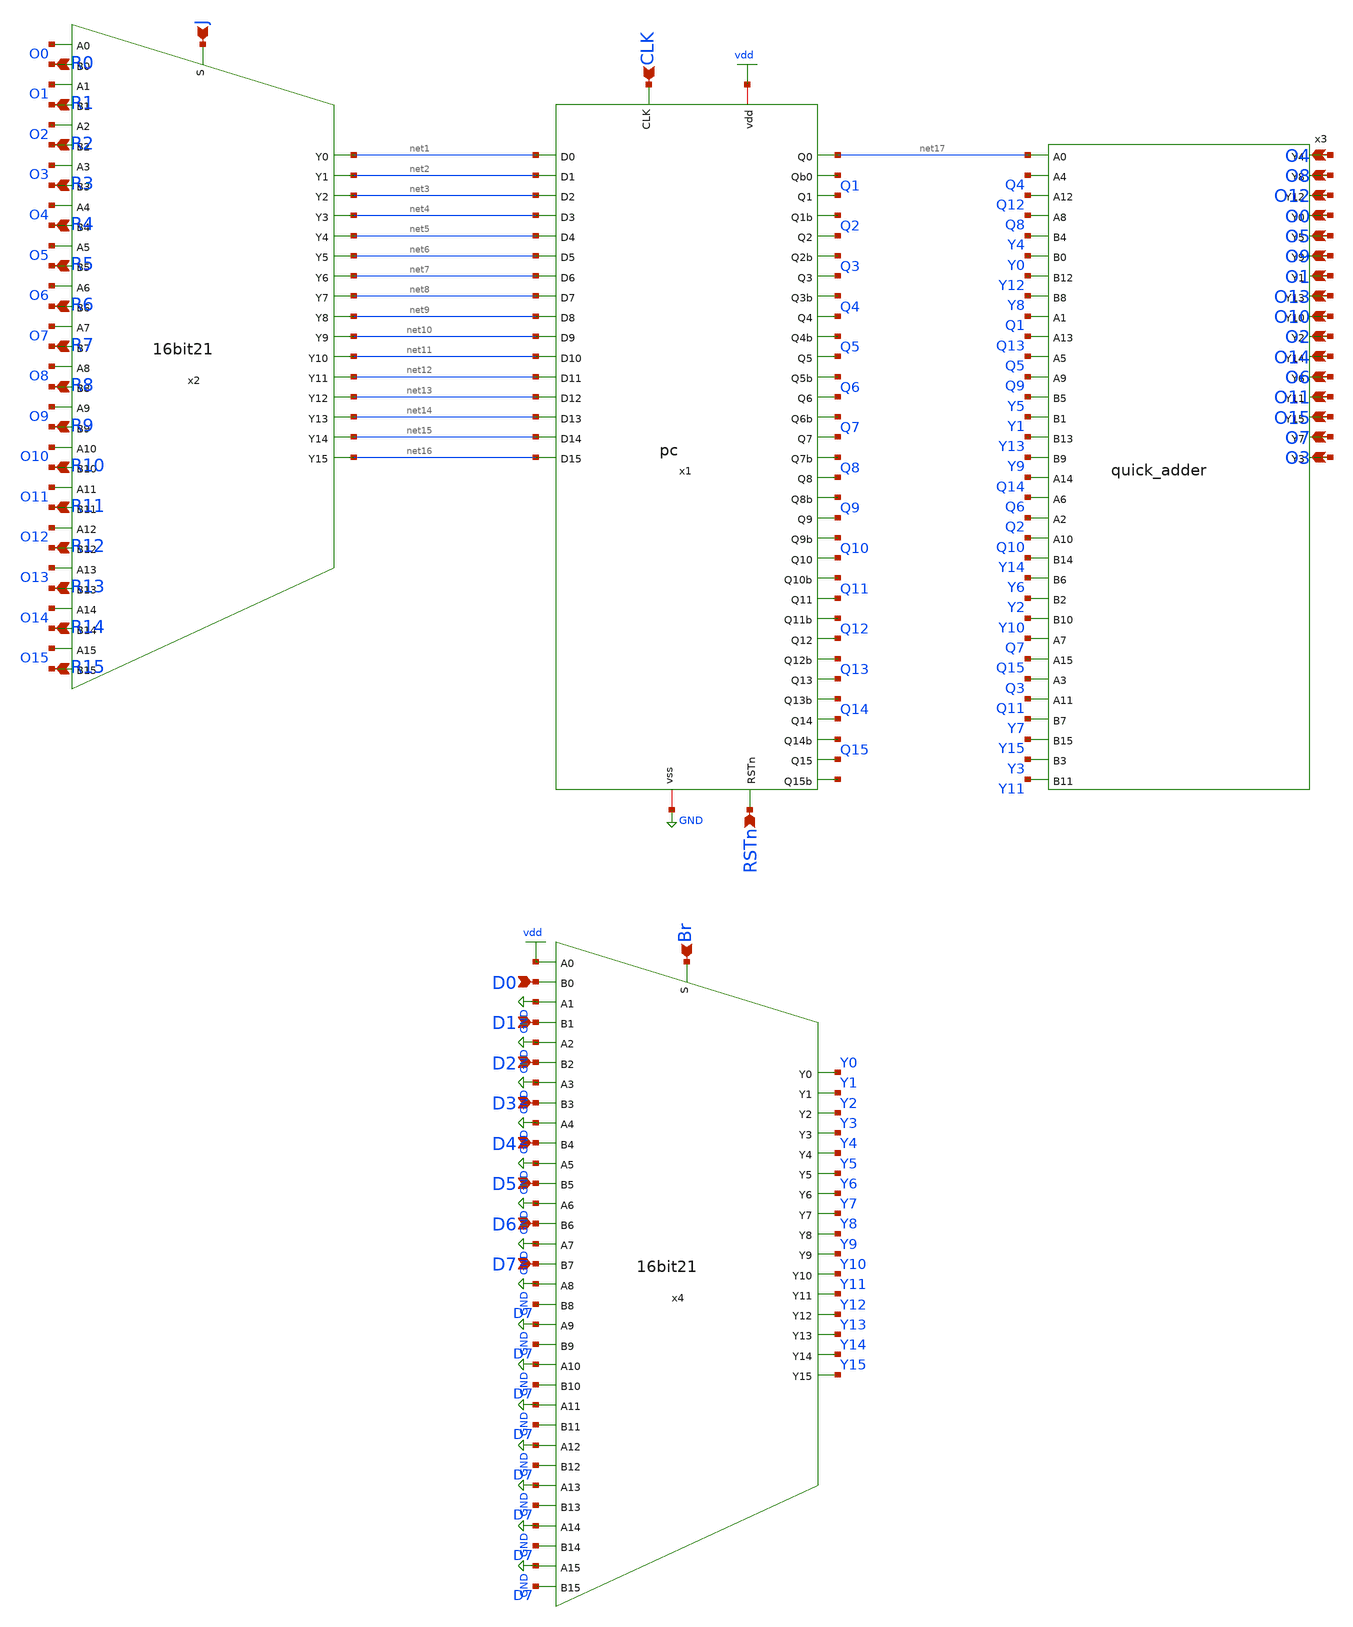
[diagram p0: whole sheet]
** sch_path: schematics/main.sch
**.subckt main J Br D0 D1 D2 D3 D4 D5 D6 D7 RSTn O4 O8 O12 O0 O5 O9 O1 O13 O10 O2 O14 O6 O11 O15 O7
*+ O3 CLK R0 R1 R2 R3 R4 R5 R6 R7 R8 R9 R10 R11 R12 R13 R14 R15
*.ipin J
*.ipin Br
*.ipin D0
*.ipin D1
*.ipin D2
*.ipin D3
*.ipin D4
*.ipin D5
*.ipin D6
*.ipin D7
*.ipin RSTn
*.opin O4
*.opin O8
*.opin O12
*.opin O0
*.opin O5
*.opin O9
*.opin O1
*.opin O13
*.opin O10
*.opin O2
*.opin O14
*.opin O6
*.opin O11
*.opin O15
*.opin O7
*.opin O3
*.ipin CLK
*.ipin R0
*.ipin R1
*.ipin R2
*.ipin R3
*.ipin R4
*.ipin R5
*.ipin R6
*.ipin R7
*.ipin R8
*.ipin R9
*.ipin R10
*.ipin R11
*.ipin R12
*.ipin R13
*.ipin R14
*.ipin R15
x1 GND vdd net17 net1 net18 CLK RSTn Q1 net2 net19 Q2 net3 net20 Q3 net4 net21 Q4 net5 net22 Q5 net6
+ net23 Q6 net7 net24 Q7 net8 net25 Q8 net9 net26 Q9 net10 net27 Q10 net11 net28 Q11 net12 net29 Q12 net13
+ net30 Q13 net14 net31 Q14 net15 net32 Q15 net16 net33 pc
x2 J O0 net1 R0 O1 net2 R1 O2 net3 R2 O3 net4 R3 O4 net5 R4 O5 net6 R5 O6 net7 R6 O7 net8 R7 O8 net9
+ R8 O9 net10 R9 O10 net11 R10 O11 net12 R11 O12 net13 R12 O13 net14 R13 O14 net15 R14 O15 net16 R15
+ 16bit21
x3 O4 O8 net17 Q4 O12 O0 Q12 O5 Q8 Y4 O9 Y0 O1 O13 Y12 O10 Y8 Q1 O2 Q13 Q5 O14 Q9 O6 Y5 O11 O15 Y1
+ O7 Y13 O3 Y9 Q14 Q6 Q2 Q10 Y14 Y6 Y2 Y10 Q7 Q15 Q3 Q11 Y7 Y15 Y3 Y11 quick_adder
x4 Br vdd Y0 D0 GND Y1 D1 GND Y2 D2 GND Y3 D3 GND Y4 D4 GND Y5 D5 GND Y6 D6 GND Y7 D7 GND Y8 D7 GND
+ Y9 D7 GND Y10 D7 GND Y11 D7 GND Y12 D7 GND Y13 D7 GND Y14 D7 GND Y15 D7 16bit21
**.ends
.GLOBAL vdd
.GLOBAL GND
.end
